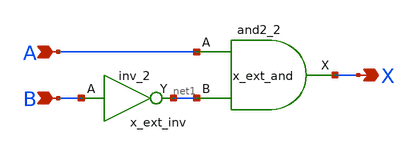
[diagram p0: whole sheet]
** sch_path: xschem/lib/phase_diff.sch
**.subckt phase_diff A B X
*.ipin A
*.ipin B
*.opin X
x_ext_and A net1 GND GND VDD VDD X sky130_fd_sc_hd__and2_2
x_ext_inv B GND GND VDD VDD net1 sky130_fd_sc_hd__inv_2
**.ends
.end
